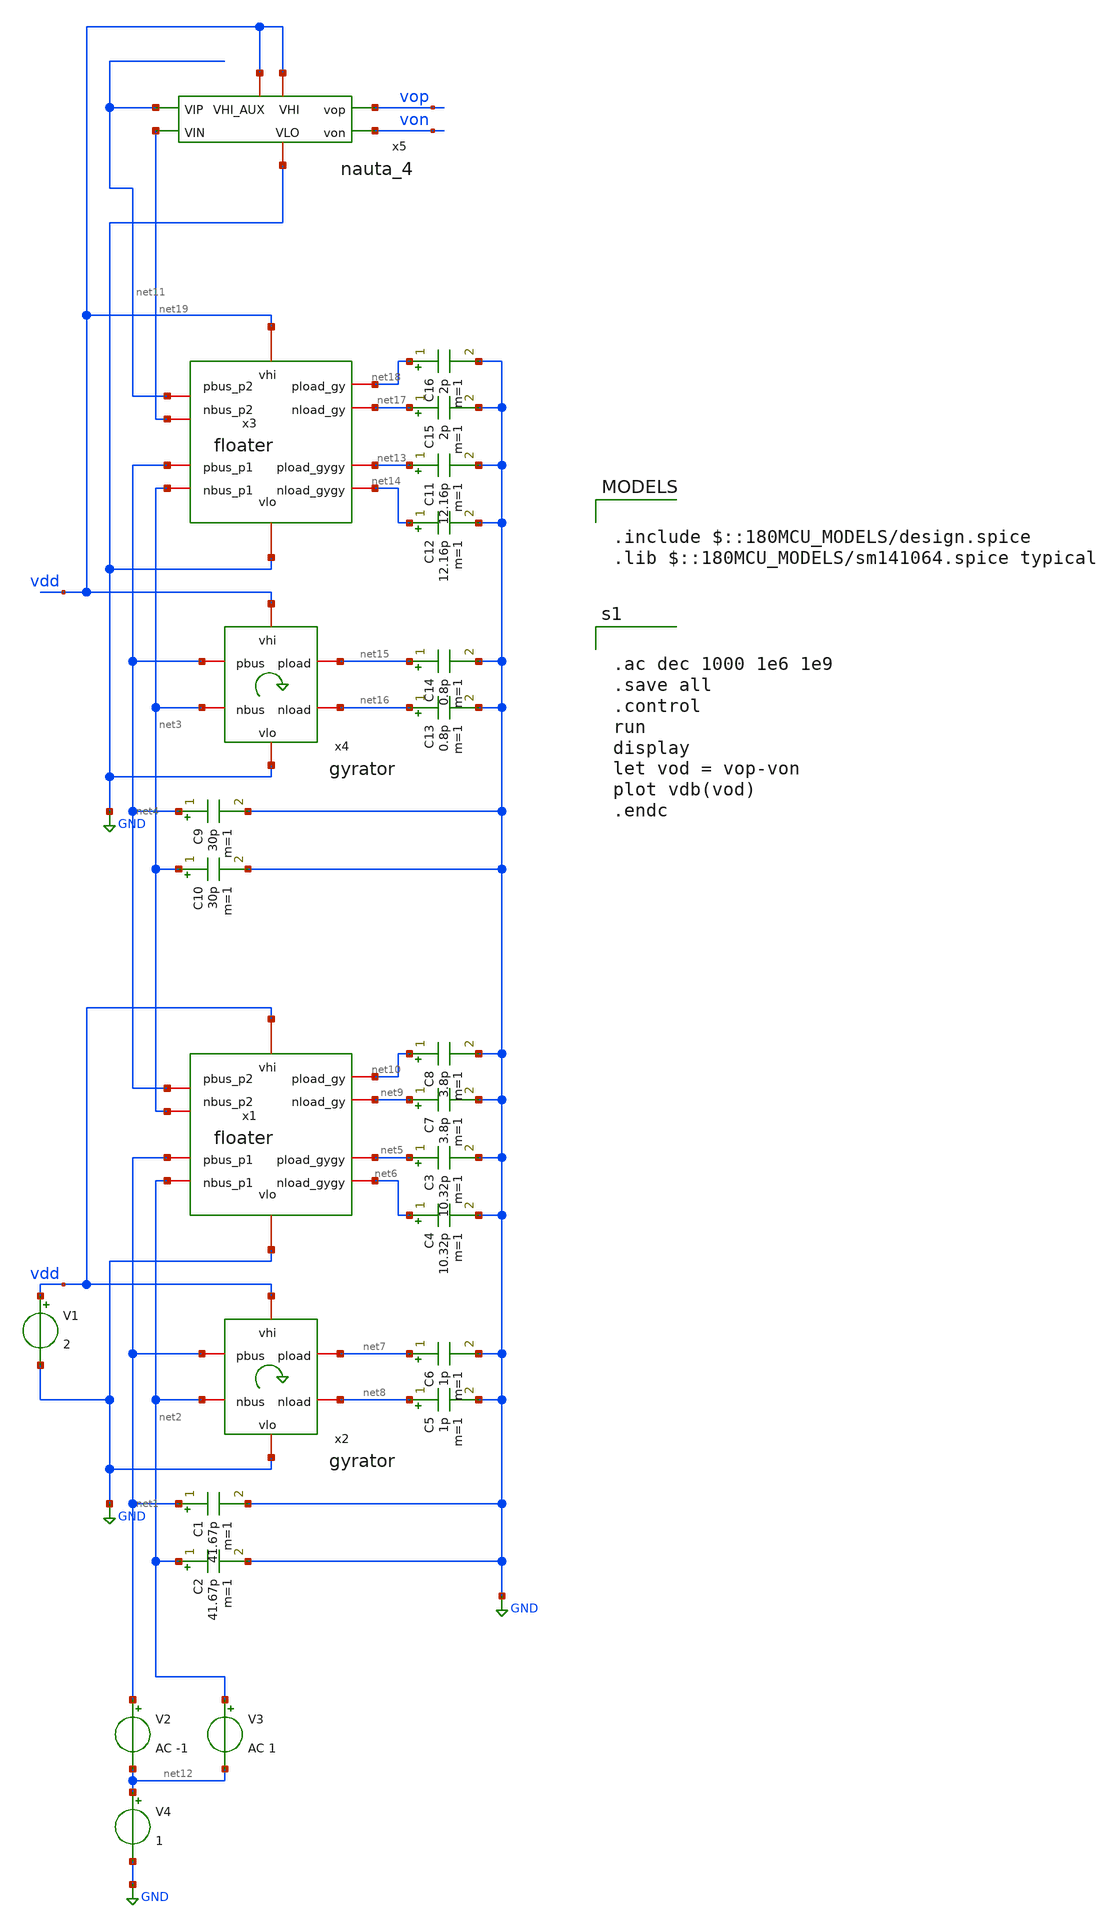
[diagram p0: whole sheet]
** sch_path: xschem/chebyshev_test_l1.sch
**.subckt chebyshev_test_l1
x1 vdd net4 net3 net9 net10 GND net6 net5 net1 net2 floater
x2 vdd net7 net1 net8 net2 GND gyrator
C1 net1 GND 41.67p m=1
C2 net2 GND 41.67p m=1
C3 net5 GND 10.32p m=1
C4 net6 GND 10.32p m=1
C5 net8 GND 1p m=1
C6 net7 GND 1p m=1
C7 net9 GND 3.8p m=1
C8 net10 GND 3.8p m=1
V1 vdd GND 2
V2 net1 net12 AC -1
V3 net2 net12 AC 1
V4 net12 GND 1
x3 vdd net11 net19 net17 net18 GND net14 net13 net4 net3 floater
x4 vdd net15 net4 net16 net3 GND gyrator
C10 net3 GND 30p m=1
C12 net14 GND 12.16p m=1
C13 net16 GND 0.8p m=1
C14 net15 GND 0.8p m=1
C15 net17 GND 2p m=1
C16 net18 GND 2p m=1
C9 net4 GND 30p m=1
C11 net13 GND 12.16p m=1
x5 vdd vdd net11 vop net19 von GND nauta_4
**** begin user architecture code


.ac dec 1000 1e6 1e9
.save all
.control
run
display
let vod = vop-von
plot vdb(vod)
.endc



.include $::180MCU_MODELS/design.spice
.lib $::180MCU_MODELS/sm141064.spice typical

**** end user architecture code
**.ends

* expanding   symbol:  floater.sym # of pins=10
** sym_path: xschem/floater.sym
** sch_path: xschem/floater.sch
.subckt floater vhi pbus_p2 nbus_p2 nload_gy pload_gy vlo nload_gygy pload_gygy pbus_p1 nbus_p1
*.iopin nbus_p1
*.iopin pbus_p1
*.iopin nbus_p2
*.iopin pbus_p2
*.iopin vhi
*.iopin vlo
*.iopin pload_gy
*.iopin nload_gy
*.iopin pload_gygy
*.iopin nload_gygy
x1 vhi vhi nbus_p2 pload_gy pbus_p2 nload_gy vlo nauta_4
x2 vhi vhi nload_gy nbus_p2 pload_gy nbus_p1 vlo nauta_4
x3 vhi vhi pload_gy pbus_p2 nload_gy pbus_p1 vlo nauta_4
x4 vhi vhi nbus_p1 nload_gy pbus_p1 pload_gy vlo nauta_4
x5 vhi nload_gygy nload_gy pload_gygy pload_gy vlo gyrator
x6 vhi vhi nbus_p2 pload_gy pbus_p2 nload_gy vlo nauta_4
x7 vhi vhi nbus_p2 pload_gy pbus_p2 nload_gy vlo nauta_4
x8 vhi vhi nbus_p2 pload_gy pbus_p2 nload_gy vlo nauta_4
x9 vhi vhi nbus_p2 pload_gy pbus_p2 nload_gy vlo nauta_4
x10 vhi vhi nload_gy nbus_p2 pload_gy nbus_p1 vlo nauta_4
x11 vhi vhi nload_gy nbus_p2 pload_gy nbus_p1 vlo nauta_4
x12 vhi vhi nload_gy nbus_p2 pload_gy nbus_p1 vlo nauta_4
x13 vhi vhi nload_gy nbus_p2 pload_gy nbus_p1 vlo nauta_4
x14 vhi vhi pload_gy pbus_p2 nload_gy pbus_p1 vlo nauta_4
x15 vhi vhi pload_gy pbus_p2 nload_gy pbus_p1 vlo nauta_4
x16 vhi vhi pload_gy pbus_p2 nload_gy pbus_p1 vlo nauta_4
x17 vhi vhi pload_gy pbus_p2 nload_gy pbus_p1 vlo nauta_4
x18 vhi vhi nbus_p1 nload_gy pbus_p1 pload_gy vlo nauta_4
x19 vhi vhi nbus_p1 nload_gy pbus_p1 pload_gy vlo nauta_4
x20 vhi vhi nbus_p1 nload_gy pbus_p1 pload_gy vlo nauta_4
x21 vhi vhi nbus_p1 nload_gy pbus_p1 pload_gy vlo nauta_4
.ends


* expanding   symbol:  gyrator.sym # of pins=6
** sym_path: xschem/gyrator.sym
** sch_path: xschem/gyrator.sch
.subckt gyrator vhi pload pbus nload nbus vlo
*.iopin nbus
*.iopin pbus
*.iopin vhi
*.iopin vlo
*.iopin pload
*.iopin nload
x1 vhi vhi pbus pload nbus nload vlo nauta_4
x2 vhi vhi nload pbus pload nbus vlo nauta_4
x3 vhi vhi pbus pload nbus nload vlo nauta_4
x4 vhi vhi pbus pload nbus nload vlo nauta_4
x5 vhi vhi pbus pload nbus nload vlo nauta_4
x6 vhi vhi pbus pload nbus nload vlo nauta_4
x7 vhi vhi nload pbus pload nbus vlo nauta_4
x8 vhi vhi nload pbus pload nbus vlo nauta_4
x9 vhi vhi nload pbus pload nbus vlo nauta_4
x10 vhi vhi nload pbus pload nbus vlo nauta_4
.ends


* expanding   symbol:  nauta_4.sym # of pins=7
** sym_path: xschem/nauta_4.sym
** sch_path: xschem/nauta_4.sch
.subckt nauta_4 VHI_AUX VHI VIP vop VIN von VLO
*.ipin VIP
*.ipin VIN
*.opin vop
*.opin von
*.iopin VHI
*.iopin VHI_AUX
*.iopin VLO
**** begin user architecture code

.subckt NAUTA VOP VON VIP VIN VHI VHI_AUX VLO

XA0N VON VIP VLO VLO nmos_6p0 w=0.82u l=0.6u
XA0P VON VIP VHI VHI pmos_6p0 w=1.22u l=0.5u
XA1N VON VIP VLO VLO nmos_6p0 w=0.82u l=0.6u
XA1P VON VIP VHI VHI pmos_6p0 w=1.22u l=0.5u

XB0N VOP VIN VLO VLO nmos_6p0 w=0.82u l=0.6u
XB0P VOP VIN VHI VHI pmos_6p0 w=1.22u l=0.5u
XB1N VOP VIN VLO VLO nmos_6p0 w=0.82u l=0.6u
XB1P VOP VIN VHI VHI pmos_6p0 w=1.22u l=0.5u

XC0N VOP VON VLO VLO nmos_6p0 w=0.82u l=0.6u
XC0P VOP VON VHI VHI pmos_6p0 w=1.22u l=0.5u

XD0N VON VOP VLO VLO nmos_6p0 w=0.82u l=0.6u
XD0P VON VOP VHI VHI pmos_6p0 w=1.22u l=0.5u

XC1N VOP VOP VLO VLO nmos_6p0 w=0.82u l=0.6u
XC1P VOP VOP VHI_AUX VHI_AUX pmos_6p0 w=1.22u l=0.5u

XD1N VON VON VLO VLO nmos_6p0 w=0.82u l=0.6u
XD1P VON VON VHI_AUX VHI_AUX pmos_6p0 w=1.22u l=0.5u

.ends

XDUT VOP VON VIP VIN VHI VHI_AUX VLO NAUTA


**** end user architecture code
.ends

.GLOBAL GND
.end
